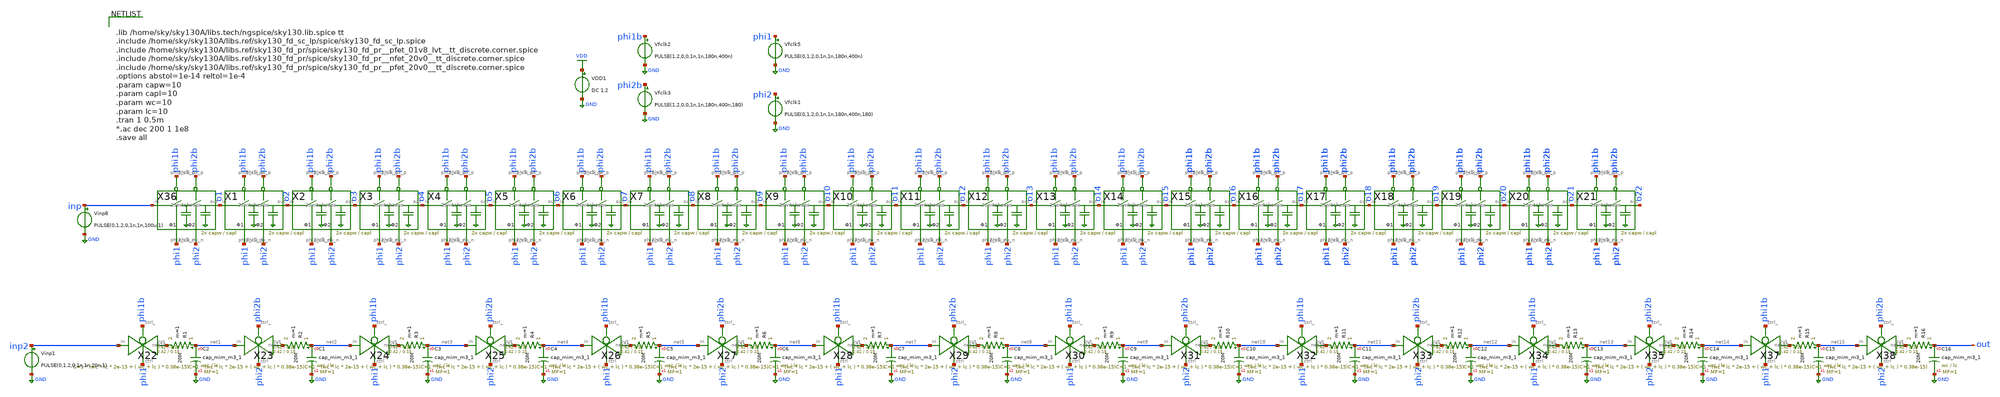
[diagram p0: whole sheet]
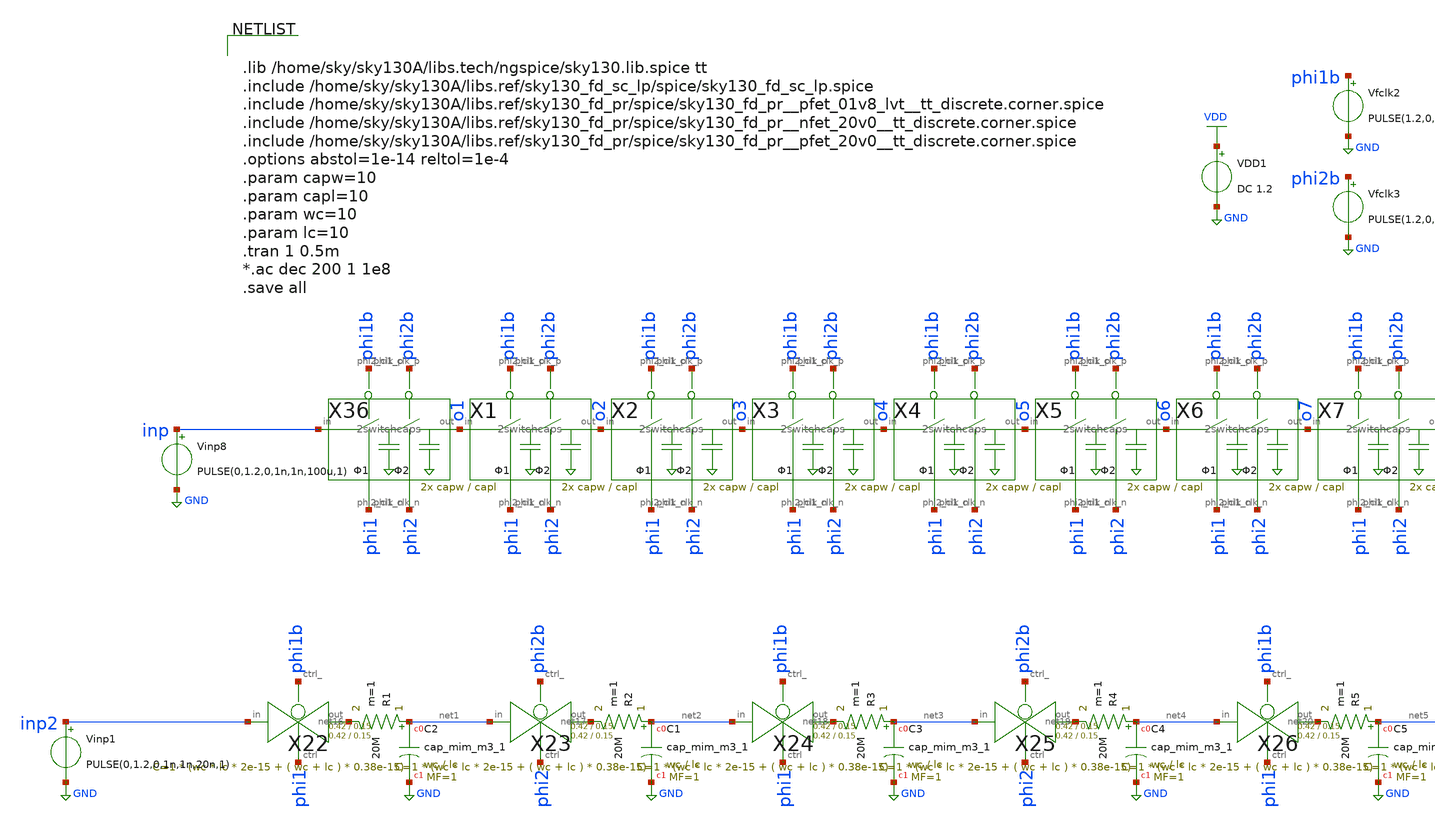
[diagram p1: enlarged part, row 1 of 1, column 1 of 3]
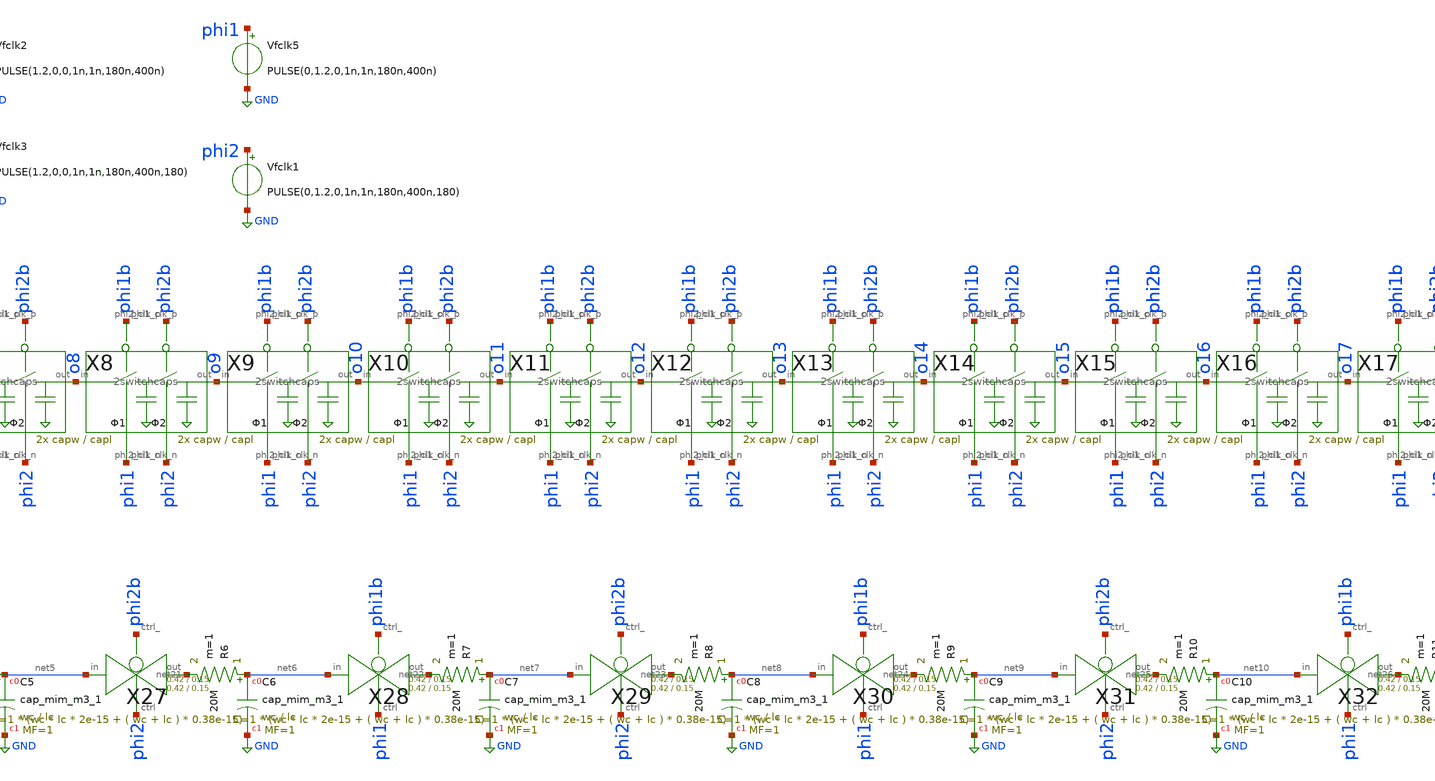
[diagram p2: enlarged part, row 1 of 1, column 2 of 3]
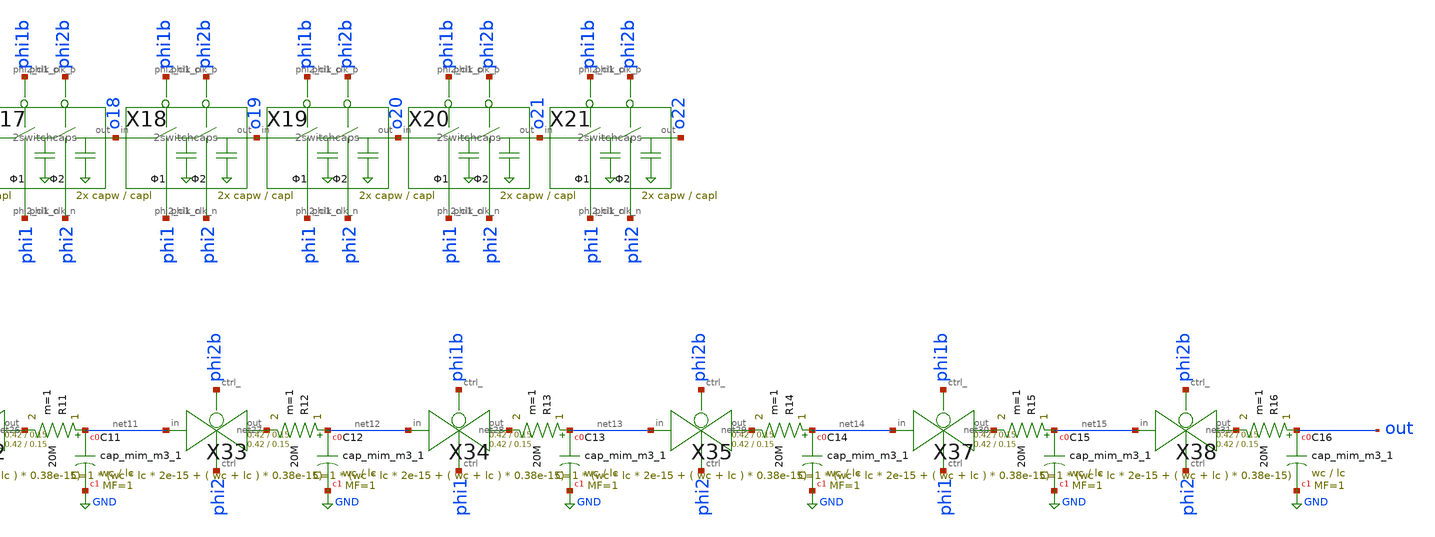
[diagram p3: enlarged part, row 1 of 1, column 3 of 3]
** sch_path: xschem/comparator_with_AZ/gauss.sch
**.subckt gauss
X36 inp o1 phi2 phi1 phi1b phi2b 2switchcaps Wcap=capw Lcap=capl
X1 o1 o2 phi2 phi1 phi1b phi2b 2switchcaps Wcap=capw Lcap=capl
X2 o2 o3 phi2 phi1 phi1b phi2b 2switchcaps Wcap=capw Lcap=capl
X3 o3 o4 phi2 phi1 phi1b phi2b 2switchcaps Wcap=capw Lcap=capl
X4 o4 o5 phi2 phi1 phi1b phi2b 2switchcaps Wcap=capw Lcap=capl
X5 o5 o6 phi2 phi1 phi1b phi2b 2switchcaps Wcap=capw Lcap=capl
X6 o6 o7 phi2 phi1 phi1b phi2b 2switchcaps Wcap=capw Lcap=capl
X7 o7 o8 phi2 phi1 phi1b phi2b 2switchcaps Wcap=capw Lcap=capl
X8 o8 o9 phi2 phi1 phi1b phi2b 2switchcaps Wcap=capw Lcap=capl
X9 o9 o10 phi2 phi1 phi1b phi2b 2switchcaps Wcap=capw Lcap=capl
X10 o10 o11 phi2 phi1 phi1b phi2b 2switchcaps Wcap=capw Lcap=capl
X11 o11 o12 phi2 phi1 phi1b phi2b 2switchcaps Wcap=capw Lcap=capl
X12 o12 o13 phi2 phi1 phi1b phi2b 2switchcaps Wcap=capw Lcap=capl
X13 o13 o14 phi2 phi1 phi1b phi2b 2switchcaps Wcap=capw Lcap=capl
X14 o14 o15 phi2 phi1 phi1b phi2b 2switchcaps Wcap=capw Lcap=capl
X15 o15 o16 phi2 phi1 phi1b phi2b 2switchcaps Wcap=capw Lcap=capl
VDD1 VDD GND DC 1.2
Vfclk5 phi1 GND PULSE(0,1.2,0,1n,1n,180n,400n)
Vfclk1 phi2 GND PULSE(0,1.2,0,1n,1n,180n,400n,180)
Vfclk2 phi1b GND PULSE(1.2,0,0,1n,1n,180n,400n)
Vfclk3 phi2b GND PULSE(1.2,0,0,1n,1n,180n,400n,180)
Vinp8 inp GND PULSE(0,1.2,0,1n,1n,100u,1)
X16 o16 o17 phi2 phi1 phi1b phi2b 2switchcaps Wcap=capw Lcap=capl
X17 o17 o18 phi2 phi1 phi1b phi2b 2switchcaps Wcap=capw Lcap=capl
X18 o18 o19 phi2 phi1 phi1b phi2b 2switchcaps Wcap=capw Lcap=capl
X19 o19 o20 phi2 phi1 phi1b phi2b 2switchcaps Wcap=capw Lcap=capl
X20 o20 o21 phi2 phi1 phi1b phi2b 2switchcaps Wcap=capw Lcap=capl
X21 o21 o22 phi2 phi1 phi1b phi2b 2switchcaps Wcap=capw Lcap=capl
XC2 net1 GND sky130_fd_pr__cap_mim_m3_1 W=wc L=lc MF=1 m=1
X22 inp2 net16 phi1b phi1 transmission_gate Wpmos=0.42 Lpmos=0.15 Wnmos=0.42 Lnmos=0.15
R1 net1 net16 20M m=1
X23 net1 net17 phi2b phi2 transmission_gate Wpmos=0.42 Lpmos=0.15 Wnmos=0.42 Lnmos=0.15
R2 net2 net17 20M m=1
X24 net2 net18 phi1b phi1 transmission_gate Wpmos=0.42 Lpmos=0.15 Wnmos=0.42 Lnmos=0.15
R3 net3 net18 20M m=1
X25 net3 net19 phi2b phi2 transmission_gate Wpmos=0.42 Lpmos=0.15 Wnmos=0.42 Lnmos=0.15
R4 net4 net19 20M m=1
X26 net4 net20 phi1b phi1 transmission_gate Wpmos=0.42 Lpmos=0.15 Wnmos=0.42 Lnmos=0.15
R5 net5 net20 20M m=1
X27 net5 net21 phi2b phi2 transmission_gate Wpmos=0.42 Lpmos=0.15 Wnmos=0.42 Lnmos=0.15
R6 net6 net21 20M m=1
X28 net6 net22 phi1b phi1 transmission_gate Wpmos=0.42 Lpmos=0.15 Wnmos=0.42 Lnmos=0.15
R7 net7 net22 20M m=1
X29 net7 net23 phi2b phi2 transmission_gate Wpmos=0.42 Lpmos=0.15 Wnmos=0.42 Lnmos=0.15
R8 net8 net23 20M m=1
X30 net8 net24 phi1b phi1 transmission_gate Wpmos=0.42 Lpmos=0.15 Wnmos=0.42 Lnmos=0.15
R9 net9 net24 20M m=1
X31 net9 net25 phi2b phi2 transmission_gate Wpmos=0.42 Lpmos=0.15 Wnmos=0.42 Lnmos=0.15
R10 net10 net25 20M m=1
X32 net10 net26 phi1b phi1 transmission_gate Wpmos=0.42 Lpmos=0.15 Wnmos=0.42 Lnmos=0.15
R11 net11 net26 20M m=1
X33 net11 net27 phi2b phi2 transmission_gate Wpmos=0.42 Lpmos=0.15 Wnmos=0.42 Lnmos=0.15
R12 net12 net27 20M m=1
X34 net12 net28 phi1b phi1 transmission_gate Wpmos=0.42 Lpmos=0.15 Wnmos=0.42 Lnmos=0.15
R13 net13 net28 20M m=1
X35 net13 net29 phi2b phi2 transmission_gate Wpmos=0.42 Lpmos=0.15 Wnmos=0.42 Lnmos=0.15
R14 net14 net29 20M m=1
X37 net14 net30 phi1b phi1 transmission_gate Wpmos=0.42 Lpmos=0.15 Wnmos=0.42 Lnmos=0.15
R15 net15 net30 20M m=1
X38 net15 net31 phi2b phi2 transmission_gate Wpmos=0.42 Lpmos=0.15 Wnmos=0.42 Lnmos=0.15
R16 out net31 20M m=1
Vinp1 inp2 GND PULSE(0,1.2,0,1n,1n,20n,1)
XC1 net2 GND sky130_fd_pr__cap_mim_m3_1 W=wc L=lc MF=1 m=1
XC3 net3 GND sky130_fd_pr__cap_mim_m3_1 W=wc L=lc MF=1 m=1
XC4 net4 GND sky130_fd_pr__cap_mim_m3_1 W=wc L=lc MF=1 m=1
XC5 net5 GND sky130_fd_pr__cap_mim_m3_1 W=wc L=lc MF=1 m=1
XC6 net6 GND sky130_fd_pr__cap_mim_m3_1 W=wc L=lc MF=1 m=1
XC7 net7 GND sky130_fd_pr__cap_mim_m3_1 W=wc L=lc MF=1 m=1
XC8 net8 GND sky130_fd_pr__cap_mim_m3_1 W=wc L=lc MF=1 m=1
XC9 net9 GND sky130_fd_pr__cap_mim_m3_1 W=wc L=lc MF=1 m=1
XC10 net10 GND sky130_fd_pr__cap_mim_m3_1 W=wc L=lc MF=1 m=1
XC11 net11 GND sky130_fd_pr__cap_mim_m3_1 W=wc L=lc MF=1 m=1
XC12 net12 GND sky130_fd_pr__cap_mim_m3_1 W=wc L=lc MF=1 m=1
XC13 net13 GND sky130_fd_pr__cap_mim_m3_1 W=wc L=lc MF=1 m=1
XC14 net14 GND sky130_fd_pr__cap_mim_m3_1 W=wc L=lc MF=1 m=1
XC15 net15 GND sky130_fd_pr__cap_mim_m3_1 W=wc L=lc MF=1 m=1
XC16 out GND sky130_fd_pr__cap_mim_m3_1 W=wc L=lc MF=1 m=1
**** begin user architecture code


.lib /home/sky/sky130A/libs.tech/ngspice/sky130.lib.spice tt
.include /home/sky/sky130A/libs.ref/sky130_fd_sc_lp/spice/sky130_fd_sc_lp.spice
.include /home/sky/sky130A/libs.ref/sky130_fd_pr/spice/sky130_fd_pr__pfet_01v8_lvt__tt_discrete.corner.spice
.include /home/sky/sky130A/libs.ref/sky130_fd_pr/spice/sky130_fd_pr__nfet_20v0__tt_discrete.corner.spice
.include /home/sky/sky130A/libs.ref/sky130_fd_pr/spice/sky130_fd_pr__pfet_20v0__tt_discrete.corner.spice
.options abstol=1e-14 reltol=1e-4
.param capw=10
.param capl=10
.param wc=10
.param lc=10
.tran 1 0.5m
*.ac dec 200 1 1e8
.save all


**** end user architecture code
**.ends

* expanding   symbol:  tryandtest/2switchcaps.sym # of pins=6
** sym_path: xschem/comparator_with_AZ/2switchcaps.sym
** sch_path: xschem/comparator_with_AZ/2switchcaps.sch
.subckt 2switchcaps in out phi2_clk_n phi1_clk_n phi1_clk_p phi2_clk_p  Wcap=20 Lcap=20
*.iopin out
*.iopin in
*.ipin phi1_clk_n
*.ipin phi1_clk_p
*.ipin phi2_clk_p
*.ipin phi2_clk_n
XC1 c1 GND sky130_fd_pr__cap_mim_m3_1 W=3 L=3 MF=1 m=1
XC2 out GND sky130_fd_pr__cap_mim_m3_1 W=Wcap L=Lcap MF=1 m=1
**** begin user architecture code

.ic v(c1)=0 v(out)=0

**** end user architecture code
X1 in c1 phi1_clk_p phi1_clk_n transmission_gate Wpmos=0.42 Lpmos=0.15 Wnmos=0.42 Lnmos=0.15
X2 c1 out phi2_clk_p phi2_clk_n transmission_gate Wpmos=0.42 Lpmos=0.15 Wnmos=0.42 Lnmos=0.15
.ends


* expanding   symbol:  transmission_gate/transmission_gate.sym # of pins=4
** sym_path: xschem/transmission_gate/transmission_gate.sym
** sch_path: xschem/transmission_gate/transmission_gate.sch
.subckt transmission_gate in out ctrl_ ctrl  Wpmos=0.42 Lpmos=0.18 Wnmos=0.42 Lnmos=0.18
*.iopin in
*.iopin out
*.ipin ctrl_
*.ipin ctrl
XM1 out ctrl in GND sky130_fd_pr__nfet_01v8 L=Lnmos W=Wnmos nf=1 ad='int((nf+1)/2) * W/nf * 0.29' as='int((nf+2)/2) * W/nf * 0.29'
+ pd='2*int((nf+1)/2) * (W/nf + 0.29)' ps='2*int((nf+2)/2) * (W/nf + 0.29)' nrd='0.29 / W' nrs='0.29 / W'
+ sa=0 sb=0 sd=0 mult=1 m=1
XM2 out ctrl_ in VDD sky130_fd_pr__pfet_01v8 L=Lpmos W=Wpmos nf=1 ad='int((nf+1)/2) * W/nf * 0.29' as='int((nf+2)/2) * W/nf * 0.29'
+ pd='2*int((nf+1)/2) * (W/nf + 0.29)' ps='2*int((nf+2)/2) * (W/nf + 0.29)' nrd='0.29 / W' nrs='0.29 / W'
+ sa=0 sb=0 sd=0 mult=1 m=1
.ends

.GLOBAL GND
.GLOBAL VDD
.end
